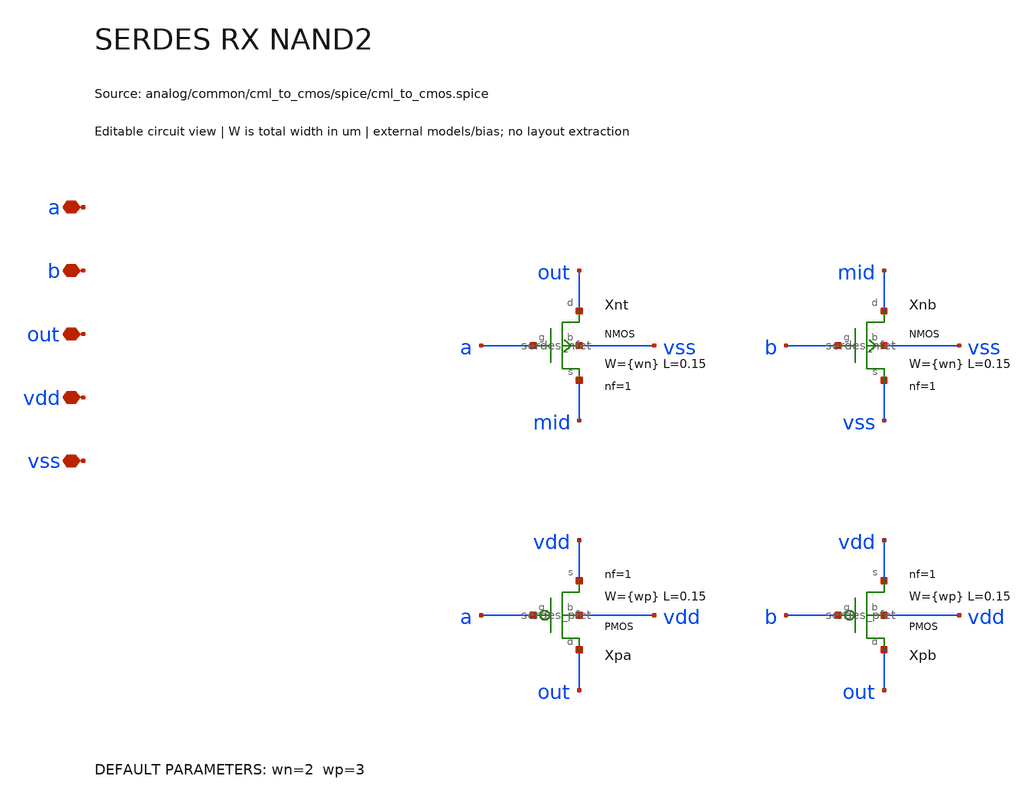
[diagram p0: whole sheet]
** sch_path: analog/common/cml_to_cmos/schematic/serdes_rx_nand2.sch
**.subckt serdes_rx_nand2 a b out vdd vss
*.iopin a
*.iopin b
*.iopin out
*.iopin vdd
*.iopin vss
Xnt out a mid vss serdes_nfet w={wn} l=0.15 nf=1
Xnb mid b vss vss serdes_nfet w={wn} l=0.15 nf=1
Xpa out a vdd vdd serdes_pfet w={wp} l=0.15 nf=1
Xpb out b vdd vdd serdes_pfet w={wp} l=0.15 nf=1
**.ends

* expanding   symbol:  serdes/serdes_nfet.sym # of pins=4
** sym_path: analog/common/devices/schematic/serdes_nfet.sym
** sch_path: analog/common/devices/schematic/serdes_nfet.sch
.subckt serdes_nfet d g s b  w=1 l=0.15 nf=1
*.iopin d
*.iopin g
*.iopin s
*.iopin b
Xmos d g s b sky130_fd_pr__nfet_01v8 w={w} l={l} nf={nf} ad={floor((nf+1)/2)*(w/nf)*0.29} as={floor((nf+2)/2)*(w/nf)*0.29}
+ pd={2*floor((nf+1)/2)*(w/nf+0.29)} ps={2*floor((nf+2)/2)*(w/nf+0.29)}
.ends


* expanding   symbol:  serdes/serdes_pfet.sym # of pins=4
** sym_path: analog/common/devices/schematic/serdes_pfet.sym
** sch_path: analog/common/devices/schematic/serdes_pfet.sch
.subckt serdes_pfet d g s b  w=3 l=0.15 nf=1
*.iopin d
*.iopin g
*.iopin s
*.iopin b
Xmos d g s b sky130_fd_pr__pfet_01v8 w={w} l={l} nf={nf} ad={floor((nf+1)/2)*(w/nf)*0.29} as={floor((nf+2)/2)*(w/nf)*0.29}
+ pd={2*floor((nf+1)/2)*(w/nf+0.29)} ps={2*floor((nf+2)/2)*(w/nf+0.29)}
.ends

.end
